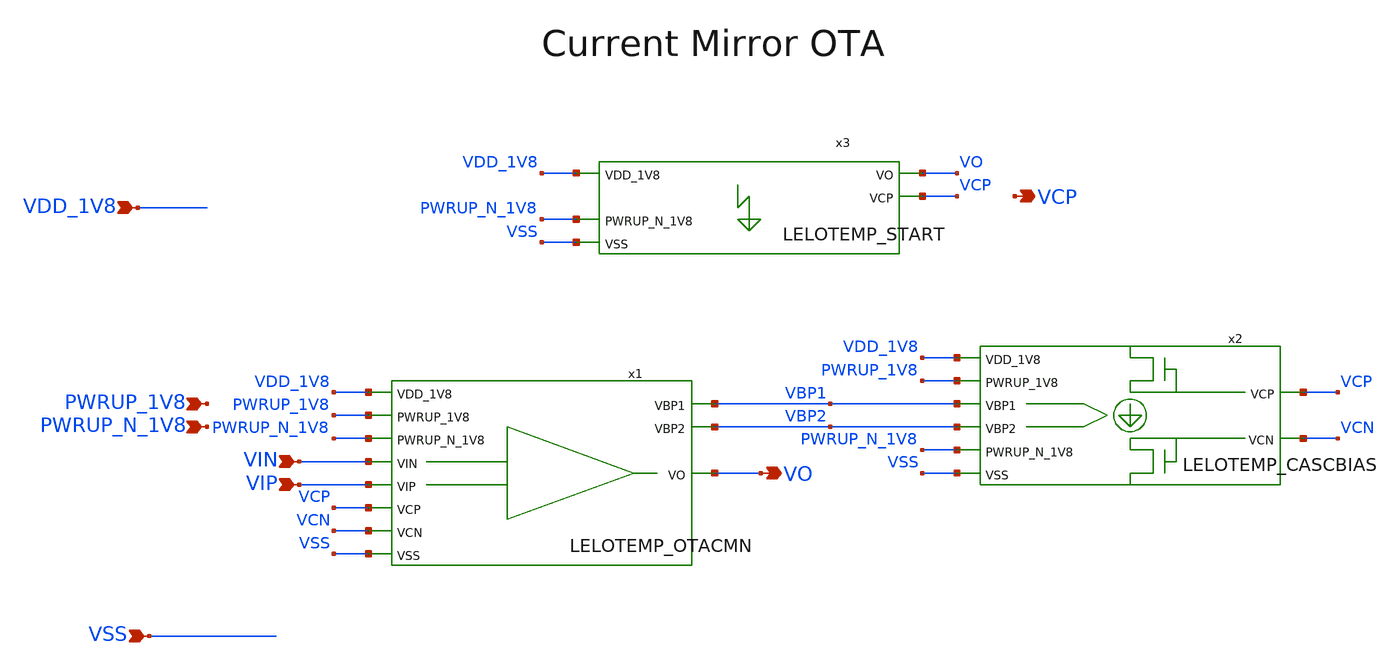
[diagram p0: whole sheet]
** sch_path: design/LELO_TEMP_SKY130A/LELOTEMP_OTAN.sch
**.subckt LELOTEMP_OTAN VDD_1V8 VSS PWRUP_N_1V8 PWRUP_1V8 VO VIP VIN VCP
*.ipin VDD_1V8
*.ipin VSS
*.ipin PWRUP_N_1V8
*.ipin PWRUP_1V8
*.opin VO
*.ipin VIP
*.ipin VIN
*.opin VCP
x1 VDD_1V8 PWRUP_1V8 VCP VO VCN PWRUP_N_1V8 VIN VIP VSS VBP1 VBP2 LELOTEMP_OTACMN
x2 VDD_1V8 PWRUP_1V8 VCN VCP VBP1 VBP2 PWRUP_N_1V8 VSS LELOTEMP_CASCBIAS
x3 VDD_1V8 VO VCP PWRUP_N_1V8 VSS LELOTEMP_START
**.ends
.end
